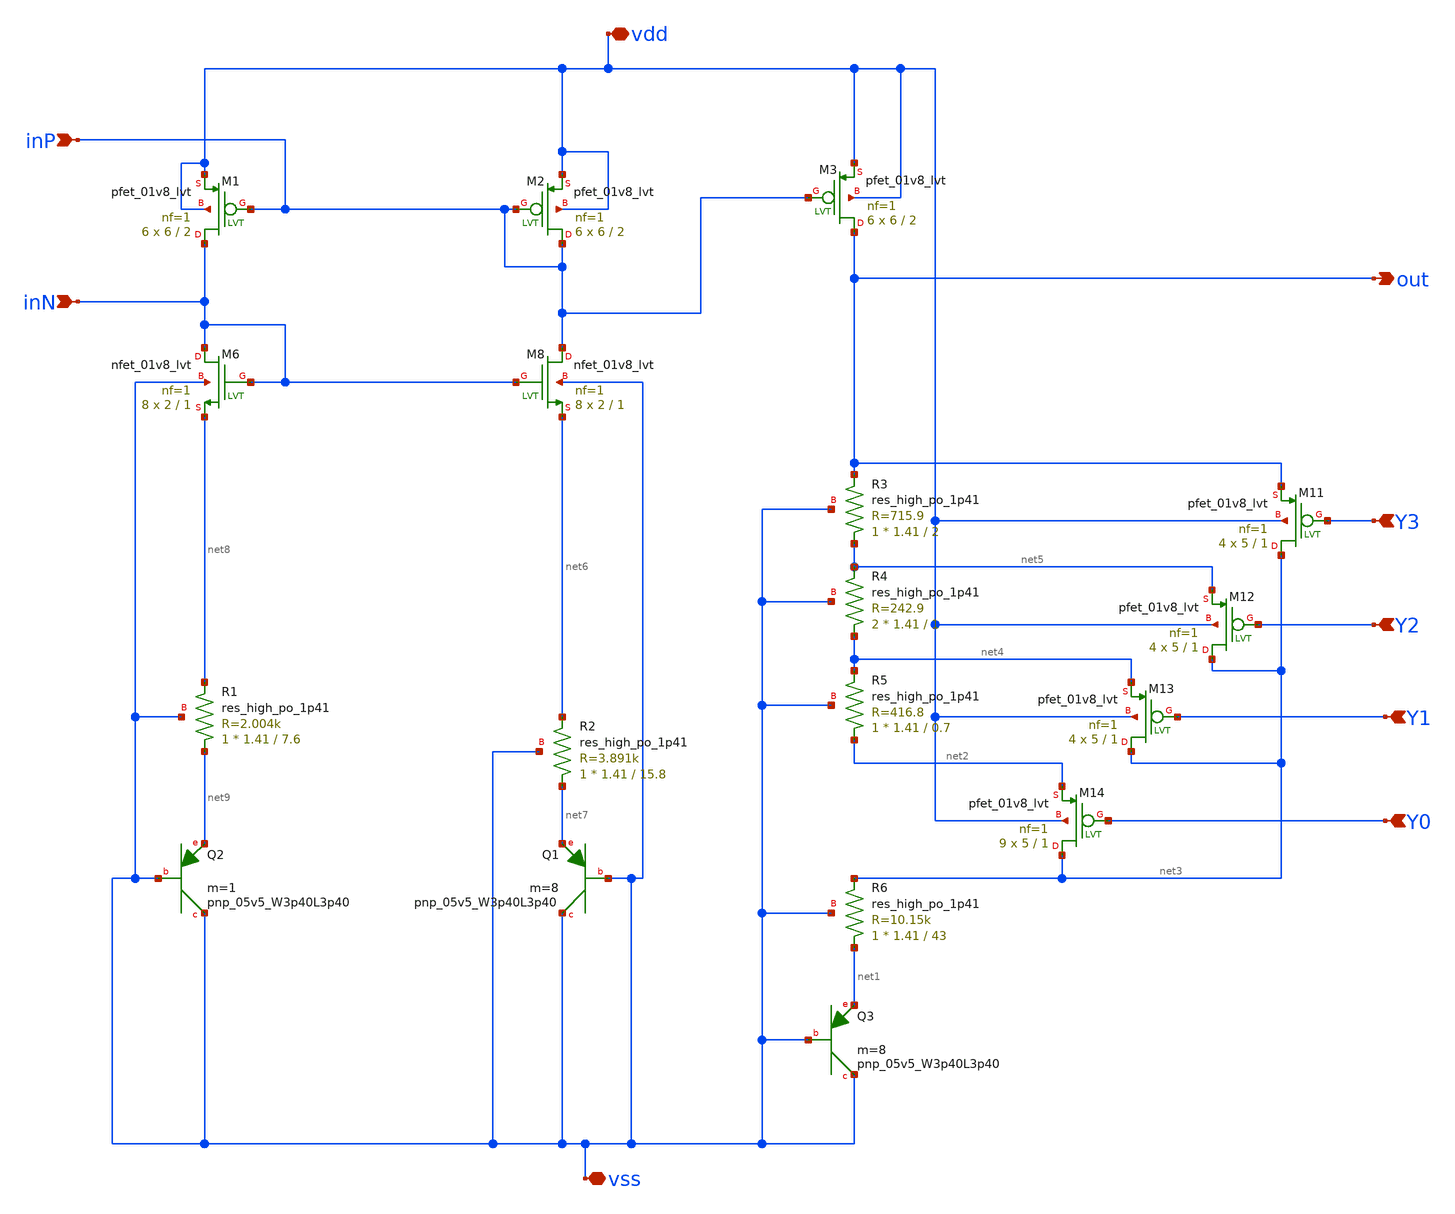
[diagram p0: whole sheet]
** sch_path: BGR_coreAndVrefBranch.sch
**.subckt BGR_coreAndVrefBranch out vss Y3 Y2 Y1 Y0 vdd inP inN
*.opin out
*.iopin vss
*.ipin Y3
*.ipin Y2
*.ipin Y1
*.ipin Y0
*.iopin vdd
*.ipin inP
*.ipin inN
XM3 out inP vdd vdd sky130_fd_pr__pfet_01v8_lvt L=2 W=6 nf=1 ad='int((1 + 1)/2) * 6 / 1 * 0.29' as='int((1 + 2)/2) * 6 / 1 * 0.29'
+ pd='2*int((1 + 1)/2) * (6 / 1 + 0.29)' ps='2*int((1 + 2)/2) * (6 / 1 + 0.29)' nrd='0.29 / 6 ' nrs='0.29 / 6 '
+ sa=0 sb=0 sd=0 mult=6 m=6
XQ3 vss vss net1 sky130_fd_pr__pnp_05v5_W3p40L3p40 m=8
XM11 net3 Y3 out vdd sky130_fd_pr__pfet_01v8_lvt L=1 W=5 nf=1 ad='int((1 + 1)/2) * 5 / 1 * 0.29' as='int((1 + 2)/2) * 5 / 1 * 0.29'
+ pd='2*int((1 + 1)/2) * (5 / 1 + 0.29)' ps='2*int((1 + 2)/2) * (5 / 1 + 0.29)' nrd='0.29 / 5 ' nrs='0.29 / 5 '
+ sa=0 sb=0 sd=0 mult=4 m=4
XM12 net3 Y2 net5 vdd sky130_fd_pr__pfet_01v8_lvt L=1 W=5 nf=1 ad='int((1 + 1)/2) * 5 / 1 * 0.29' as='int((1 + 2)/2) * 5 / 1 * 0.29'
+ pd='2*int((1 + 1)/2) * (5 / 1 + 0.29)' ps='2*int((1 + 2)/2) * (5 / 1 + 0.29)' nrd='0.29 / 5 ' nrs='0.29 / 5 '
+ sa=0 sb=0 sd=0 mult=4 m=4
XM13 net3 Y1 net4 vdd sky130_fd_pr__pfet_01v8_lvt L=1 W=5 nf=1 ad='int((1 + 1)/2) * 5 / 1 * 0.29' as='int((1 + 2)/2) * 5 / 1 * 0.29'
+ pd='2*int((1 + 1)/2) * (5 / 1 + 0.29)' ps='2*int((1 + 2)/2) * (5 / 1 + 0.29)' nrd='0.29 / 5 ' nrs='0.29 / 5 '
+ sa=0 sb=0 sd=0 mult=4 m=4
XM14 net3 Y0 net2 vdd sky130_fd_pr__pfet_01v8_lvt L=1 W=5 nf=1 ad='int((1 + 1)/2) * 5 / 1 * 0.29' as='int((1 + 2)/2) * 5 / 1 * 0.29'
+ pd='2*int((1 + 1)/2) * (5 / 1 + 0.29)' ps='2*int((1 + 2)/2) * (5 / 1 + 0.29)' nrd='0.29 / 5 ' nrs='0.29 / 5 '
+ sa=0 sb=0 sd=0 mult=9 m=9
XM6 inN inN net8 vss sky130_fd_pr__nfet_01v8_lvt L=1 W=2 nf=1 ad='int((1 + 1)/2) * 2 / 1 * 0.29' as='int((1 + 2)/2) * 2 / 1 * 0.29'
+ pd='2*int((1 + 1)/2) * (2 / 1 + 0.29)' ps='2*int((1 + 2)/2) * (2 / 1 + 0.29)' nrd='0.29 / 2 ' nrs='0.29 / 2 '
+ sa=0 sb=0 sd=0 mult=8 m=8
XM1 inN inP vdd vdd sky130_fd_pr__pfet_01v8_lvt L=2 W=6 nf=1 ad='int((1 + 1)/2) * 6 / 1 * 0.29' as='int((1 + 2)/2) * 6 / 1 * 0.29'
+ pd='2*int((1 + 1)/2) * (6 / 1 + 0.29)' ps='2*int((1 + 2)/2) * (6 / 1 + 0.29)' nrd='0.29 / 6 ' nrs='0.29 / 6 '
+ sa=0 sb=0 sd=0 mult=6 m=6
XQ1 vss vss net7 sky130_fd_pr__pnp_05v5_W3p40L3p40 m=8
XM2 inP inP vdd vdd sky130_fd_pr__pfet_01v8_lvt L=2 W=6 nf=1 ad='int((1 + 1)/2) * 6 / 1 * 0.29' as='int((1 + 2)/2) * 6 / 1 * 0.29'
+ pd='2*int((1 + 1)/2) * (6 / 1 + 0.29)' ps='2*int((1 + 2)/2) * (6 / 1 + 0.29)' nrd='0.29 / 6 ' nrs='0.29 / 6 '
+ sa=0 sb=0 sd=0 mult=6 m=6
XM8 inP inN net6 vss sky130_fd_pr__nfet_01v8_lvt L=1 W=2 nf=1 ad='int((1 + 1)/2) * 2 / 1 * 0.29' as='int((1 + 2)/2) * 2 / 1 * 0.29'
+ pd='2*int((1 + 1)/2) * (2 / 1 + 0.29)' ps='2*int((1 + 2)/2) * (2 / 1 + 0.29)' nrd='0.29 / 2 ' nrs='0.29 / 2 '
+ sa=0 sb=0 sd=0 mult=8 m=8
XQ2 vss vss net9 sky130_fd_pr__pnp_05v5_W3p40L3p40 m=1
XR1 net9 net8 vss sky130_fd_pr__res_high_po_1p41 L=7.6 mult=1 m=1
XR2 net7 net6 vss sky130_fd_pr__res_high_po_1p41 L=15.8 mult=1 m=1
XR3 net5 out vss sky130_fd_pr__res_high_po_1p41 L=2 mult=1 m=1
XR4 net4 net5 vss sky130_fd_pr__res_high_po_1p41 L=1 mult=2 m=2
XR5 net2 net4 vss sky130_fd_pr__res_high_po_1p41 L=0.7 mult=1 m=1
XR6 net1 net3 vss sky130_fd_pr__res_high_po_1p41 L=43 mult=1 m=1
**.ends
.end
